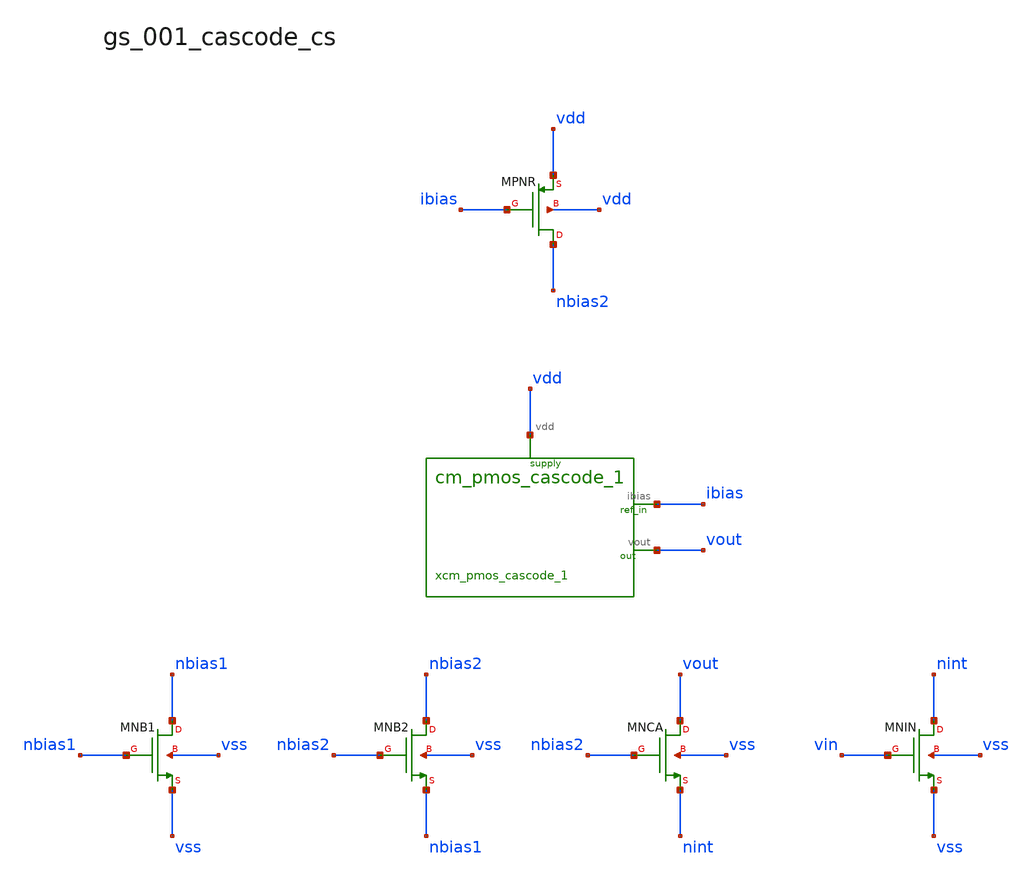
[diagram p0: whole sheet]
** sch_path: analog-db/raw/gs_001_cascode_cs/hier/gs_001_cascode_cs.sch
**.subckt gs_001_cascode_cs
xcm_pmos_cascode_1 ibias vout vdd cm_pmos_cascode_1
XMNB1 nbias1 nbias1 vss vss sg13_lv_nmos w=x_dut_xmnb1_w l=x_dut_xmnb1_l ng=1 m=x_dut_xmnb1_m
XMNB2 nbias2 nbias2 nbias1 vss sg13_lv_nmos w=x_dut_xmnb2_w l=x_dut_xmnb2_l ng=1 m=x_dut_xmnb2_m
XMNCA vout nbias2 nint vss sg13_lv_nmos w=x_dut_xmnca_w l=x_dut_xmnca_l ng=1 m=x_dut_xmnca_m
XMNIN nint vin vss vss sg13_lv_nmos w=x_dut_xmnin_w l=x_dut_xmnin_l ng=1 m=x_dut_xmnin_m
XMPNR nbias2 ibias vdd vdd sg13_lv_pmos w=x_dut_xmpnr_w l=x_dut_xmpnr_l ng=1 m=x_dut_xmpnr_m
**.ends

* expanding   symbol:  blocks/cm_pmos_cascode_1.sym # of pins=3
** sym_path: analog-db/raw/gs_001_cascode_cs/hier/blocks/cm_pmos_cascode_1.sym
** sch_path: analog-db/raw/gs_001_cascode_cs/hier/blocks/cm_pmos_cascode_1.sch
.subckt cm_pmos_cascode_1 ibias vout vdd
*.iopin vdd
*.opin ibias
*.opin vout
XMPB1 pbias1 pbias1 vdd vdd sg13_lv_pmos w=x_dut_xmpb1_w l=x_dut_xmpb1_l ng=1 m=x_dut_xmpb1_m
XMPB2 ibias ibias pbias1 vdd sg13_lv_pmos w=x_dut_xmpb2_w l=x_dut_xmpb2_l ng=1 m=x_dut_xmpb2_m
XMPCA vout ibias pint vdd sg13_lv_pmos w=x_dut_xmpca_w l=x_dut_xmpca_l ng=1 m=x_dut_xmpca_m
XMPLD pint pbias1 vdd vdd sg13_lv_pmos w=x_dut_xmpld_w l=x_dut_xmpld_l ng=1 m=x_dut_xmpld_m
.ends

.end
